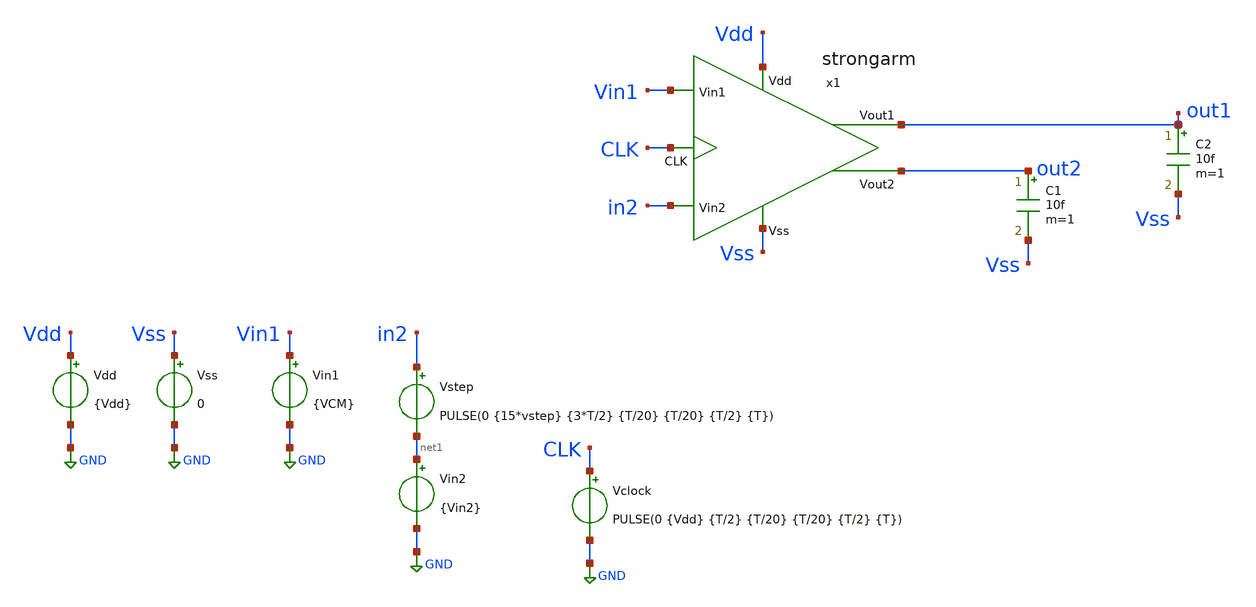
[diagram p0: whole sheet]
** sch_path: xschem/TB/TB_Tran_SA.sch
**.subckt TB_Tran_SA
Vdd Vdd GND {Vdd}
x1 out2 out1 Vdd Vss in2 Vin1 CLK strongarm
Vss Vss GND 0
C1 out2 Vss 10f m=1
C2 out1 Vss 10f m=1
Vin1 Vin1 GND {VCM}
Vin2 net1 GND {Vin2}
Vclock CLK GND PULSE(0 {Vdd} {T/2} {T/20} {T/20} {T/2} {T})
Vstep in2 net1 PULSE(0 {15*vstep} {3*T/2} {T/20} {T/20} {T/2} {T})
**** begin user architecture code


.param Vdd   = 1.8
.param VCM   = 0.9
.param Vstep = 10m
.param Vin2  = VCM-Vstep
.ic V(out1) = 1.8
.ic V(out2) = 1.8
.ic V(x1.common) = 1.8
.ic V(x1.P) = 1.8
.ic V(x1.Q) = 1.8





.lib cornerMOSlv.lib mos_tt




** TRANSISTORES NMOS

.param W12 = 5.3u
.param L12 = 0.15u
.param M12 = 1

.param W34 = 0.78u
.param L34 = 0.15u
.param M34 = 1

.param W56 = 0.78u
.param L56 = 0.15u
.param M56 = 1

.param W7  = 4u
.param L7  = 0.15u
.param M7  = 1

.param W89 = 0.5u
.param L89 = 0.15u
.param M89 = 1

.param Wab = 0.5u
.param Lab = 0.15u
.param Mab = 1





.param T = 1n
.control
*.param SimTime = 3*T + 100n
save all  @n.x1.xm3.nsg13_lv_nmos[vgs]  @n.x1.xm4.nsg13_lv_nmos[vgs]  @n.x1.xm5.nsg13_lv_pmos[vgs]
+  @n.x1.xm6.nsg13_lv_pmos[vgs]  @n.x1.xm10.nsg13_lv_pmos[vgs]  @n.x1.xm11.nsg13_lv_pmos[vgs]
*  @n.x1.xm10.nsg13_lv_pmos[vgt]  @n.x1.xm10.nsg13_lv_pmos[vth]
*  @n.x1.xm1.nsg13_lv_nmos[ids]  @n.x1.xm2.nsg13_lv_nmos[ids]  @n.x1.xm3.nsg13_lv_nmos[ids]
*+  @n.x1.xm10.nsg13_lv_pmos[ids]  @n.x1.xm11.nsg13_lv_pmos[ids]

tran 1p 3n
let vgs3 = @n.x1.xm3.nsg13_lv_nmos[vgs]
let vgs4 = @n.x1.xm4.nsg13_lv_nmos[vgs]
let vgs5 = @n.x1.xm5.nsg13_lv_pmos[vgs]
let vgs6 = @n.x1.xm6.nsg13_lv_pmos[vgs]
let vgsa = @n.x1.xm10.nsg13_lv_pmos[vgs]
let vgsb = @n.x1.xm11.nsg13_lv_pmos[vgs]

let vgta = @n.x1.xm10.nsg13_lv_pmos[vgt]
let vtha = @n.x1.xm10.nsg13_lv_pmos[vth]

let id1 = @n.x1.xm1.nsg13_lv_nmos[ids]
let id2 = @n.x1.xm2.nsg13_lv_nmos[ids]
let id10 = @n.x1.xm10.nsg13_lv_pmos[ids]
let id11 = @n.x1.xm11.nsg13_lv_pmos[ids]

meas tran Amp_t TRIG AT=15n TARG v(out1) VAL=0.9 CROSS=1
meas tran reg_t TRIG v(out1) VAL=0.9 CROSS=1 TARG v(out1) VAL=0.01 CROSS=1
meas tran Energy INTEG Pot from=15n to=25n

plot v(x1.Q) v(x1.P) v(clk)
plot v(x1.common) v(clk)
plot v(out1) v(out2)
.endc


**** end user architecture code
**.ends

* expanding   symbol:  ../sch/strongarm.sym # of pins=7
** sym_path: xschem/sch/strongarm.sym
** sch_path: xschem/sch/strongarm.sch
.subckt strongarm Vout2 Vout1 Vdd Vss Vin2 Vin1 CLK
*.opin Vout2
*.opin Vout1
*.ipin Vin1
*.ipin Vin2
*.ipin CLK
*.ipin Vss
*.ipin Vdd
XM1 common Vin1 P Vss sg13_lv_nmos w={W12} l={L12} ng=1 m={M12} mm_ok=1
XM2 common Vin2 Q Vss sg13_lv_nmos w={W12} l={L12} ng=1 m={M12} mm_ok=1
XM3 P Vout2 Vout1 Vss sg13_lv_nmos w={W34} l={L34} ng=1 m={M34} mm_ok=1
XM4 Q Vout1 Vout2 Vss sg13_lv_nmos w={W34} l={L34} ng=1 m={M34} mm_ok=1
XM6 Vout2 Vout1 Vdd Vdd sg13_lv_pmos w={W56} l={L56} ng=1 m={M56} mm_ok=1
XM5 Vout1 Vout2 Vdd Vdd sg13_lv_pmos w={W56} l={L56} ng=1 m={M56} mm_ok=1
XM7 Vss CLK common Vss sg13_lv_nmos w={W7} l={L7} ng=1 m={M7} mm_ok=1
XM8 P CLK Vdd Vdd sg13_lv_pmos w={W89} l={L89} ng=1 m={M89} mm_ok=1
XM9 Q CLK Vdd Vdd sg13_lv_pmos w={W89} l={L89} ng=1 m={M89} mm_ok=1
XM11 Vdd CLK Vout2 Vdd sg13_lv_pmos w={Wab} l={Lab} ng=1 m={Wab} mm_ok=1
XM10 Vdd CLK Vout1 Vdd sg13_lv_pmos w={Wab} l={Lab} ng=1 m={Wab} mm_ok=1
.ends

.GLOBAL GND
.end
